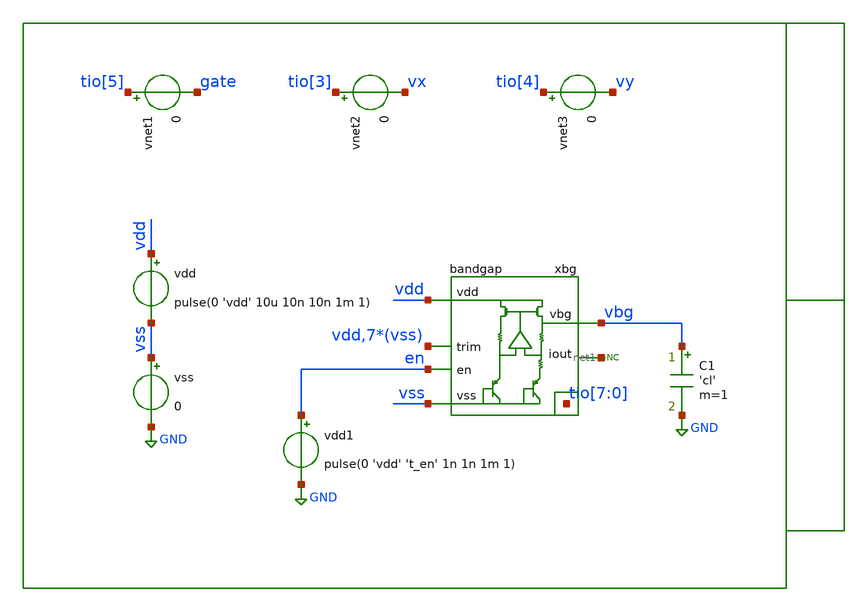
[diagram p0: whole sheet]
** sch_path: xschem/tb/bandgap_cm/bandgap/tr_bandgap_startup.sch
**.subckt tr_bandgap_startup
xbg vdd vbg vss tio[7] tio[6] tio[5] tio[4] tio[3] tio[2] tio[1] tio[0] vdd vss vss vss vss vss vss
+ vss net1 en bandgap
vss vss GND 0
C1 vbg GND 'cl' m=1
vdd vdd vss pulse(0 'vdd' 10u 10n 10n 1m 1)
vnet1 tio[5] gate 0
vnet2 tio[3] vx 0
vnet3 tio[4] vy 0
* noconn #net1
vdd1 en GND pulse(0 'vdd' 't_en' 1n 1n 1m 1)
**** begin user architecture code

* Control

.param vdd = 3.3
.param cl = 500e-15

.param t_en = 20u
.csparam t_en = t_en

.temp 27
.options reltol = 1e-6

.control
save all
tran 1u 100u

* Deviation in percent
let dev = 1

meas tran vbg_ss find v(vbg) at=99e-6

let lim_pos = vbg_ss*(1+dev/100)
let lim_neg = vbg_ss*(1-dev/100)

meas tran t_hl when v(vbg)=lim_pos fall=last
meas tran t_lh when v(vbg)=lim_neg rise=last

let t_set = max(t_hl, t_lh) - t_en

print t_set
print vbg_ss

gnuplot p1 vbg lim_pos lim_neg
gnuplot p2 vdd en vbg xbg.vs1 vx vy gate
gnuplot p3 en xbg.vs1 xbg.vs2 xbg.vs3 xbg.gate vbg

set wr_singlescale
set wr_vecnames
wrdata data.csv vbg xbg.gate xbg.vs1

.endc
.end


 * Model Corners

.include $::CORNERS/ngspice/tt.spice
*.include $::CORNERS/ngspice/ff.spice
*.include $::CORNERS/ngspice/ss.spice
*.include $::CORNERS/ngspice/sf.spice
*.include $::CORNERS/ngspice/fs.spice

**** end user architecture code
**.ends
.GLOBAL GND
.end
